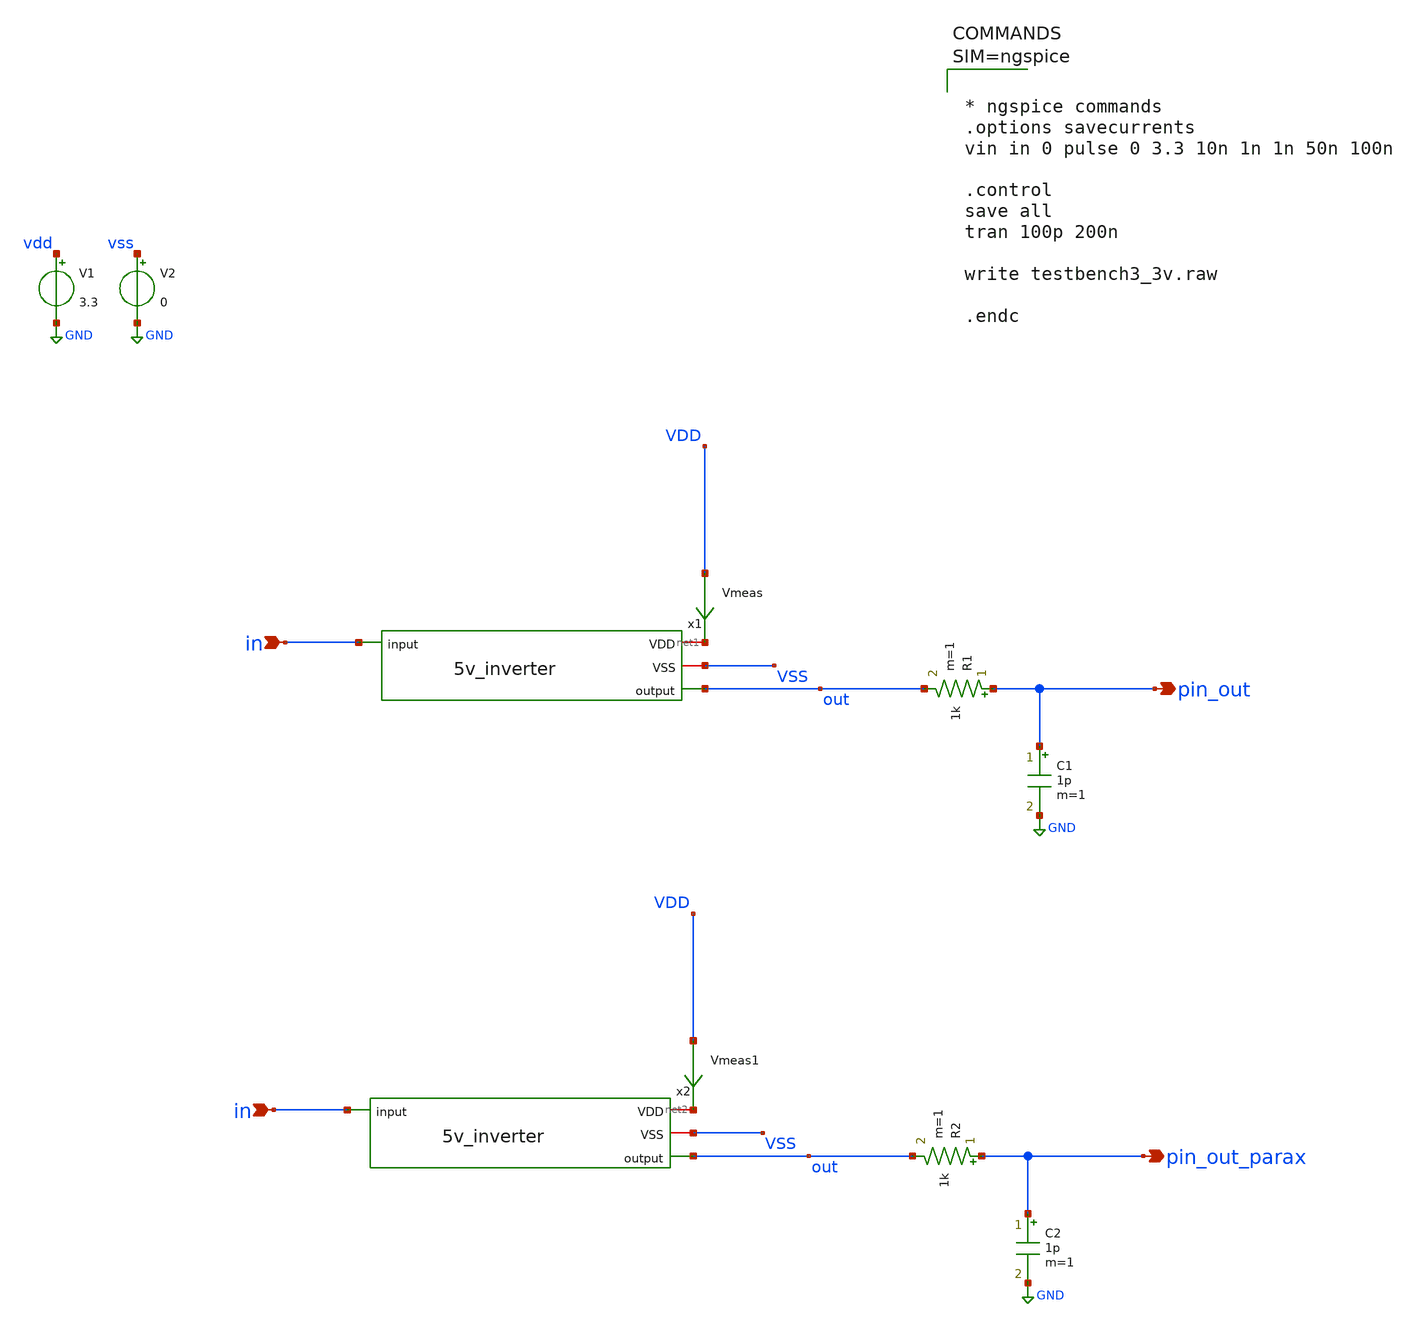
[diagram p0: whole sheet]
** sch_path: xschem/testbench3_3v.sch
**.subckt testbench3_3v pin_out in pin_out_parax in
*.opin pin_out
*.ipin in
*.opin pin_out_parax
*.ipin in
x1 net1 VSS out in 5v_inverter
V1 vdd GND 3.3
V2 vss GND 0
R1 pin_out out 1k m=1
C1 pin_out GND 1p m=1
Vmeas VDD net1 0
.save i(vmeas)
x2 net2 VSS out in 5v_inverter
R2 pin_out_parax out 1k m=1
C2 pin_out_parax GND 1p m=1
Vmeas1 VDD net2 0
.save i(vmeas1)
**** begin user architecture code



* ngspice commands
.options savecurrents
vin in 0 pulse 0 3.3 10n 1n 1n 50n 100n

.control
save all
tran 100p 200n

write testbench3_3v.raw

.endc






** opencircuitdesign pdks install
.lib $::SKYWATER_MODELS/sky130.lib.spice tt


**** end user architecture code
**.ends
.GLOBAL GND
.end
